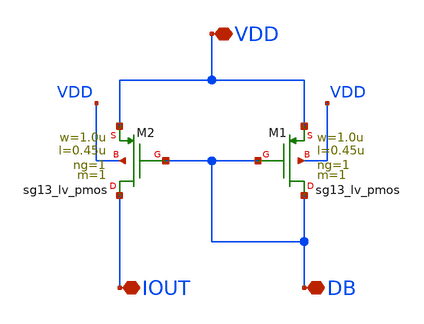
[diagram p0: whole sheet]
** sch_path: W2WDAC_Project/W2W_BOX/current_pmos.sch
**.subckt current_pmos VDD DB IOUT
*.iopin VDD
*.iopin DB
*.iopin IOUT
XM1 DB DB VDD VDD sg13_lv_pmos w=1.0u l=0.45u ng=1 m=1 mm_ok=1
XM2 IOUT DB VDD VDD sg13_lv_pmos w=1.0u l=0.45u ng=1 m=1 mm_ok=1
**.ends
.end
